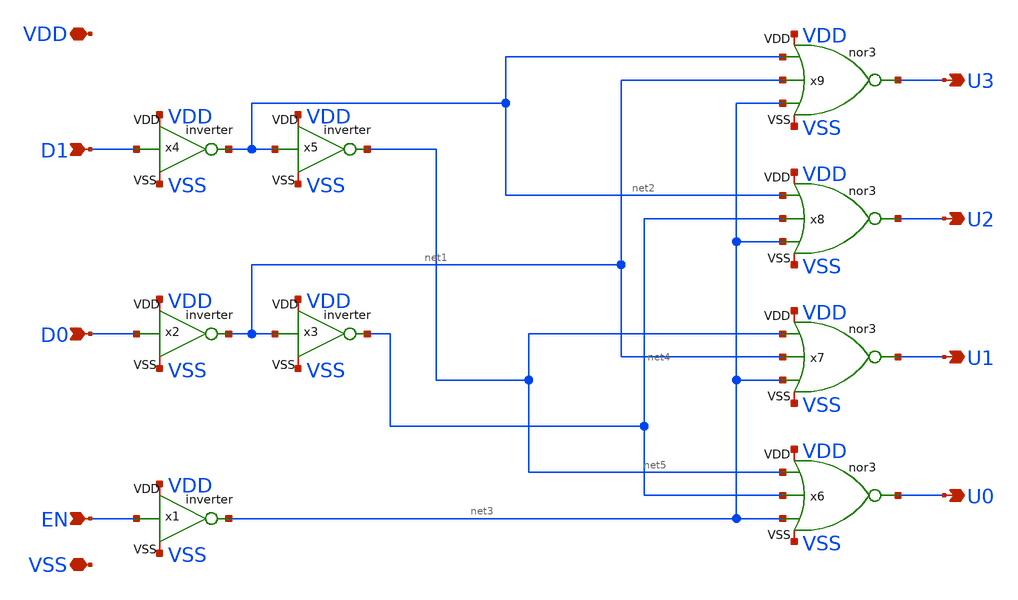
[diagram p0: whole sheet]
** sch_path: xschem/decoder2.sch
**.subckt decoder2 VDD VSS D0 D1 U0 U1 U2 U3 EN
*.iopin VDD
*.iopin VSS
*.ipin D0
*.ipin D1
*.opin U0
*.opin U1
*.opin U2
*.opin U3
*.ipin EN
x6 VDD net5 net4 U0 net3 VSS nor3
x7 VDD net5 net1 U1 net3 VSS nor3
x8 VDD net2 net4 U2 net3 VSS nor3
x9 VDD net2 net1 U3 net3 VSS nor3
x1 VDD EN net3 VSS inverter
x2 VDD D0 net1 VSS inverter
x3 VDD net1 net4 VSS inverter
x4 VDD D1 net2 VSS inverter
x5 VDD net2 net5 VSS inverter
**.ends

* expanding   symbol:  nor3.sym # of pins=6
** sym_path: xschem/nor3.sym
** sch_path: xschem/nor3.sch
.subckt nor3 VDD A B OUT C VSS
*.iopin VSS
*.iopin VDD
*.ipin B
*.ipin A
*.ipin C
*.opin OUT
XM2 OUT B VSS VSS sky130_fd_pr__nfet_g5v0d10v5 L=0.5 W=0.65 nf=1 ad='int((1 + 1)/2) * 0.65 / 1 * 0.29'
+ as='int((1 + 2)/2) * 0.65 / 1 * 0.29' pd='2*int((1 + 1)/2) * (0.65 / 1 + 0.29)' ps='2*int((1 + 2)/2) * (0.65 / 1 + 0.29)'
+ nrd='0.29 / 0.65 ' nrs='0.29 / 0.65 ' sa=0 sb=0 sd=0 mult=1 m=1
XM1 OUT A VSS VSS sky130_fd_pr__nfet_g5v0d10v5 L=0.5 W=0.65 nf=1 ad='int((1 + 1)/2) * 0.65 / 1 * 0.29'
+ as='int((1 + 2)/2) * 0.65 / 1 * 0.29' pd='2*int((1 + 1)/2) * (0.65 / 1 + 0.29)' ps='2*int((1 + 2)/2) * (0.65 / 1 + 0.29)'
+ nrd='0.29 / 0.65 ' nrs='0.29 / 0.65 ' sa=0 sb=0 sd=0 mult=1 m=1
XM4 net1 A VDD VDD sky130_fd_pr__pfet_g5v0d10v5 L=0.5 W=1 nf=1 ad='int((1 + 1)/2) * 1 / 1 * 0.29' as='int((1 + 2)/2) * 1 / 1 * 0.29'
+ pd='2*int((1 + 1)/2) * (1 / 1 + 0.29)' ps='2*int((1 + 2)/2) * (1 / 1 + 0.29)' nrd='0.29 / 1 ' nrs='0.29 / 1 '
+ sa=0 sb=0 sd=0 mult=1 m=1
XM3 OUT C VSS VSS sky130_fd_pr__nfet_g5v0d10v5 L=0.5 W=0.65 nf=1 ad='int((1 + 1)/2) * 0.65 / 1 * 0.29'
+ as='int((1 + 2)/2) * 0.65 / 1 * 0.29' pd='2*int((1 + 1)/2) * (0.65 / 1 + 0.29)' ps='2*int((1 + 2)/2) * (0.65 / 1 + 0.29)'
+ nrd='0.29 / 0.65 ' nrs='0.29 / 0.65 ' sa=0 sb=0 sd=0 mult=1 m=1
XM5 net2 B net1 VDD sky130_fd_pr__pfet_g5v0d10v5 L=0.5 W=1 nf=1 ad='int((1 + 1)/2) * 1 / 1 * 0.29' as='int((1 + 2)/2) * 1 / 1 * 0.29'
+ pd='2*int((1 + 1)/2) * (1 / 1 + 0.29)' ps='2*int((1 + 2)/2) * (1 / 1 + 0.29)' nrd='0.29 / 1 ' nrs='0.29 / 1 '
+ sa=0 sb=0 sd=0 mult=1 m=1
XM6 OUT C net2 VDD sky130_fd_pr__pfet_g5v0d10v5 L=0.5 W=1 nf=1 ad='int((1 + 1)/2) * 1 / 1 * 0.29' as='int((1 + 2)/2) * 1 / 1 * 0.29'
+ pd='2*int((1 + 1)/2) * (1 / 1 + 0.29)' ps='2*int((1 + 2)/2) * (1 / 1 + 0.29)' nrd='0.29 / 1 ' nrs='0.29 / 1 '
+ sa=0 sb=0 sd=0 mult=1 m=1
.ends


* expanding   symbol:  inverter.sym # of pins=4
** sym_path: xschem/inverter.sym
** sch_path: xschem/inverter.sch
.subckt inverter VDD IN OUT VSS
*.iopin VSS
*.iopin VDD
*.ipin IN
*.opin OUT
XM1 OUT IN VSS VSS sky130_fd_pr__nfet_g5v0d10v5 L=0.5 W=0.65 nf=1 ad='int((1 + 1)/2) * 0.65 / 1 * 0.29'
+ as='int((1 + 2)/2) * 0.65 / 1 * 0.29' pd='2*int((1 + 1)/2) * (0.65 / 1 + 0.29)' ps='2*int((1 + 2)/2) * (0.65 / 1 + 0.29)'
+ nrd='0.29 / 0.65 ' nrs='0.29 / 0.65 ' sa=0 sb=0 sd=0 mult=1 m=1
XM2 OUT IN VDD VDD sky130_fd_pr__pfet_g5v0d10v5 L=0.5 W=1 nf=1 ad='int((1 + 1)/2) * 1 / 1 * 0.29' as='int((1 + 2)/2) * 1 / 1 * 0.29'
+ pd='2*int((1 + 1)/2) * (1 / 1 + 0.29)' ps='2*int((1 + 2)/2) * (1 / 1 + 0.29)' nrd='0.29 / 1 ' nrs='0.29 / 1 '
+ sa=0 sb=0 sd=0 mult=1 m=1
.ends

.end
